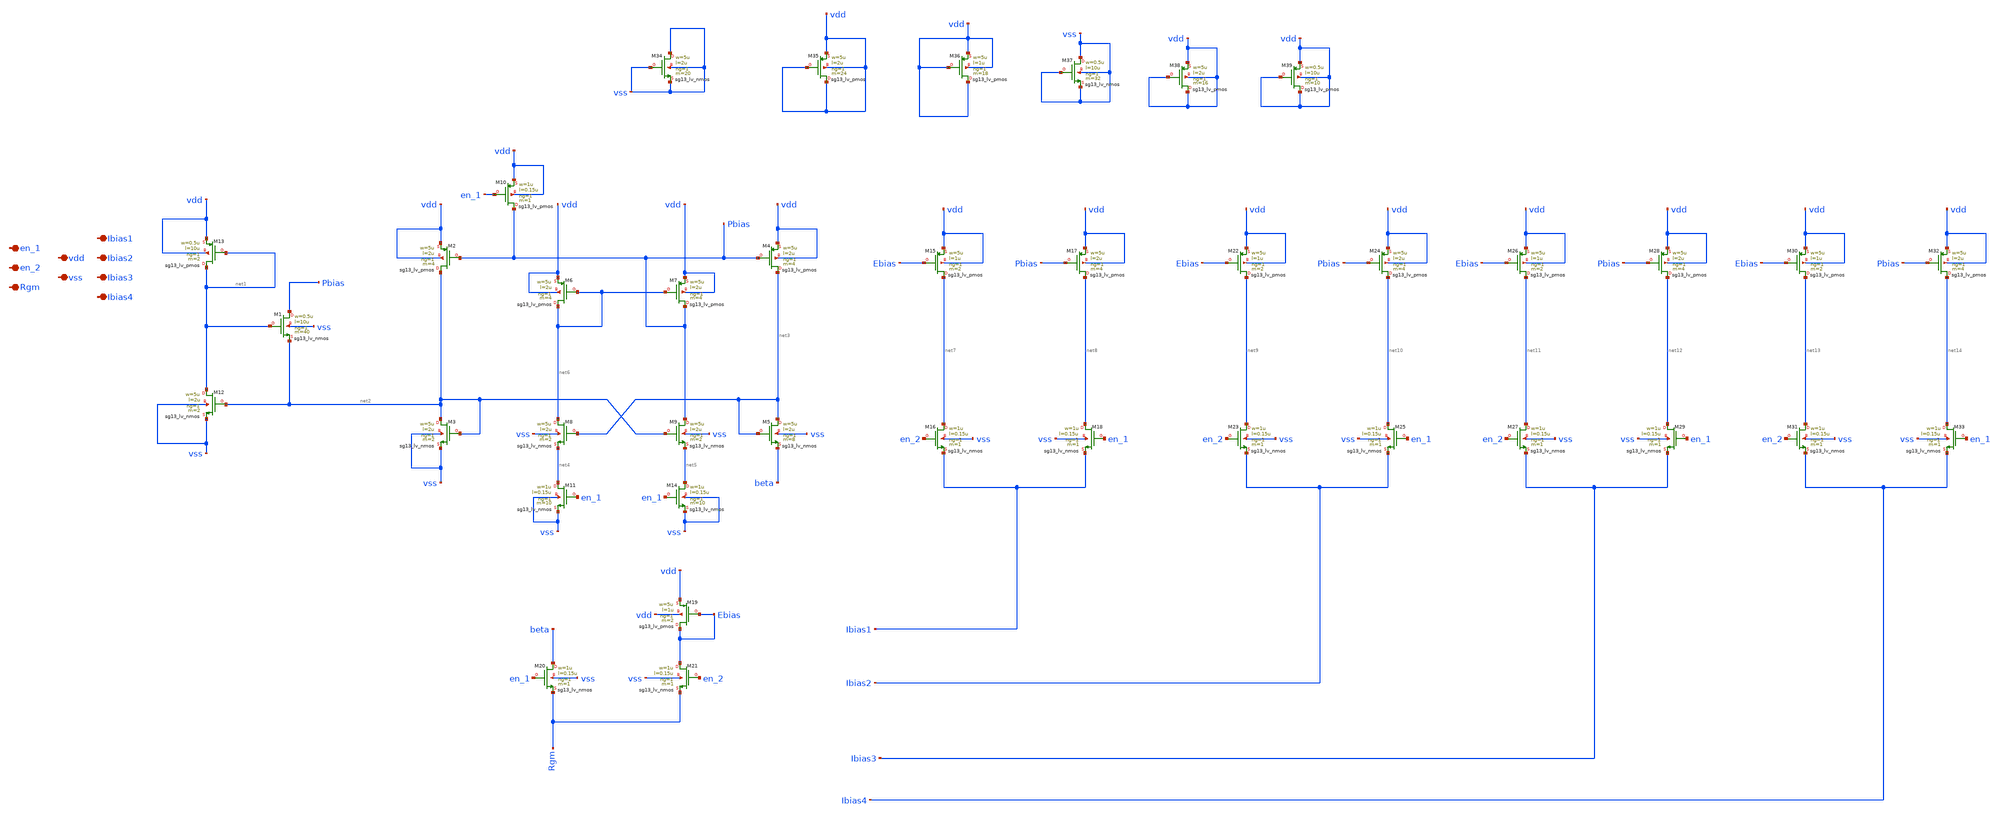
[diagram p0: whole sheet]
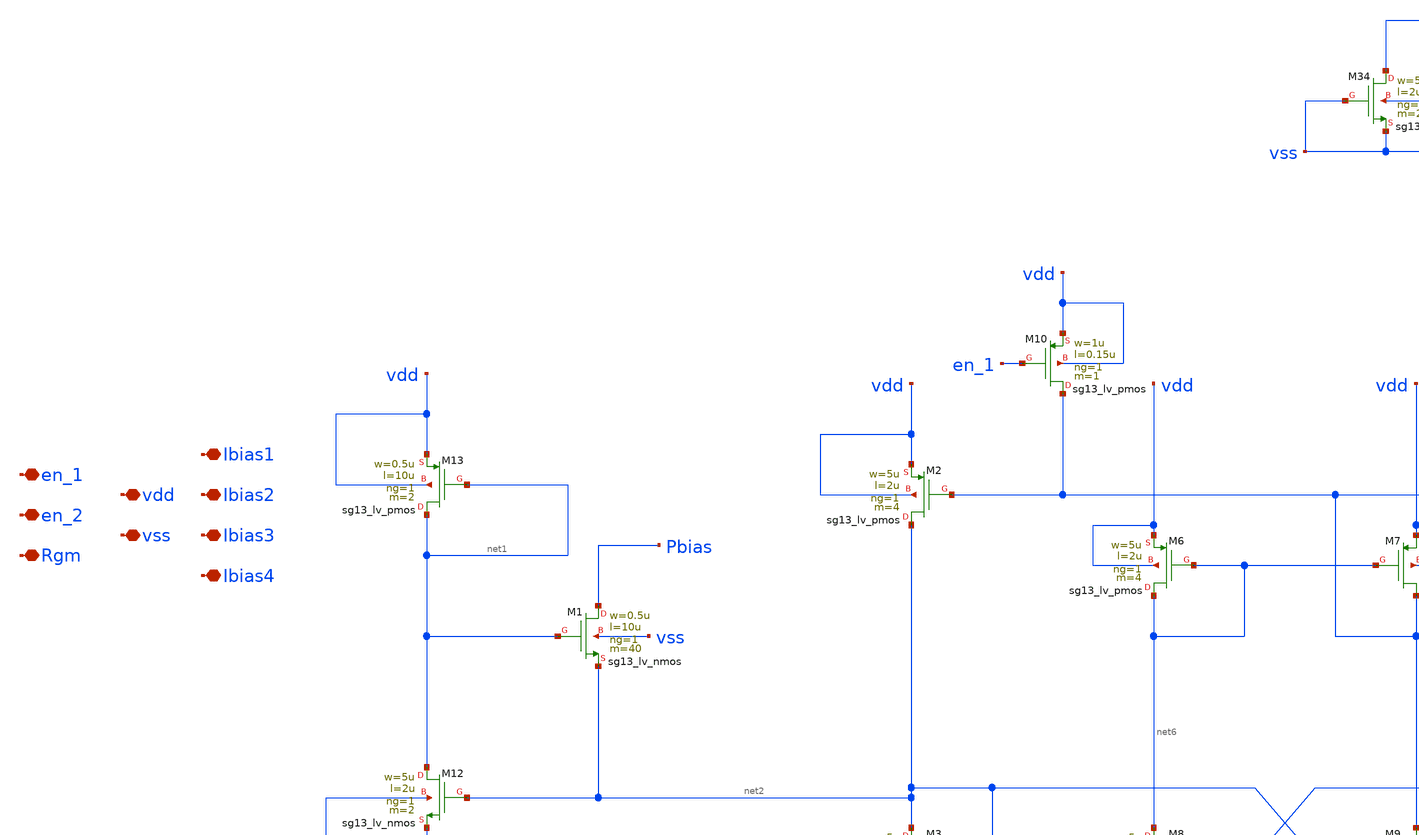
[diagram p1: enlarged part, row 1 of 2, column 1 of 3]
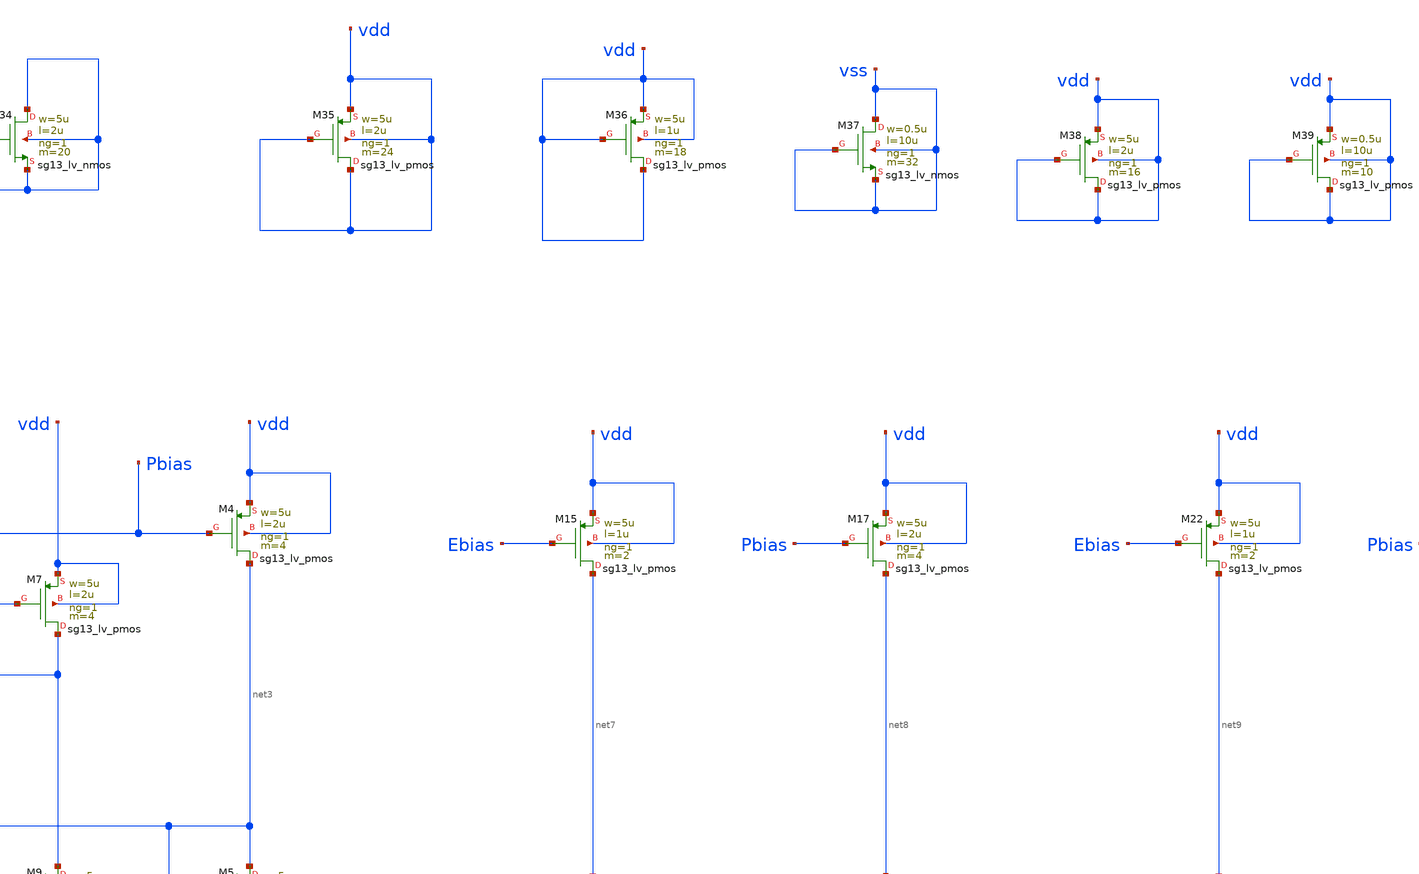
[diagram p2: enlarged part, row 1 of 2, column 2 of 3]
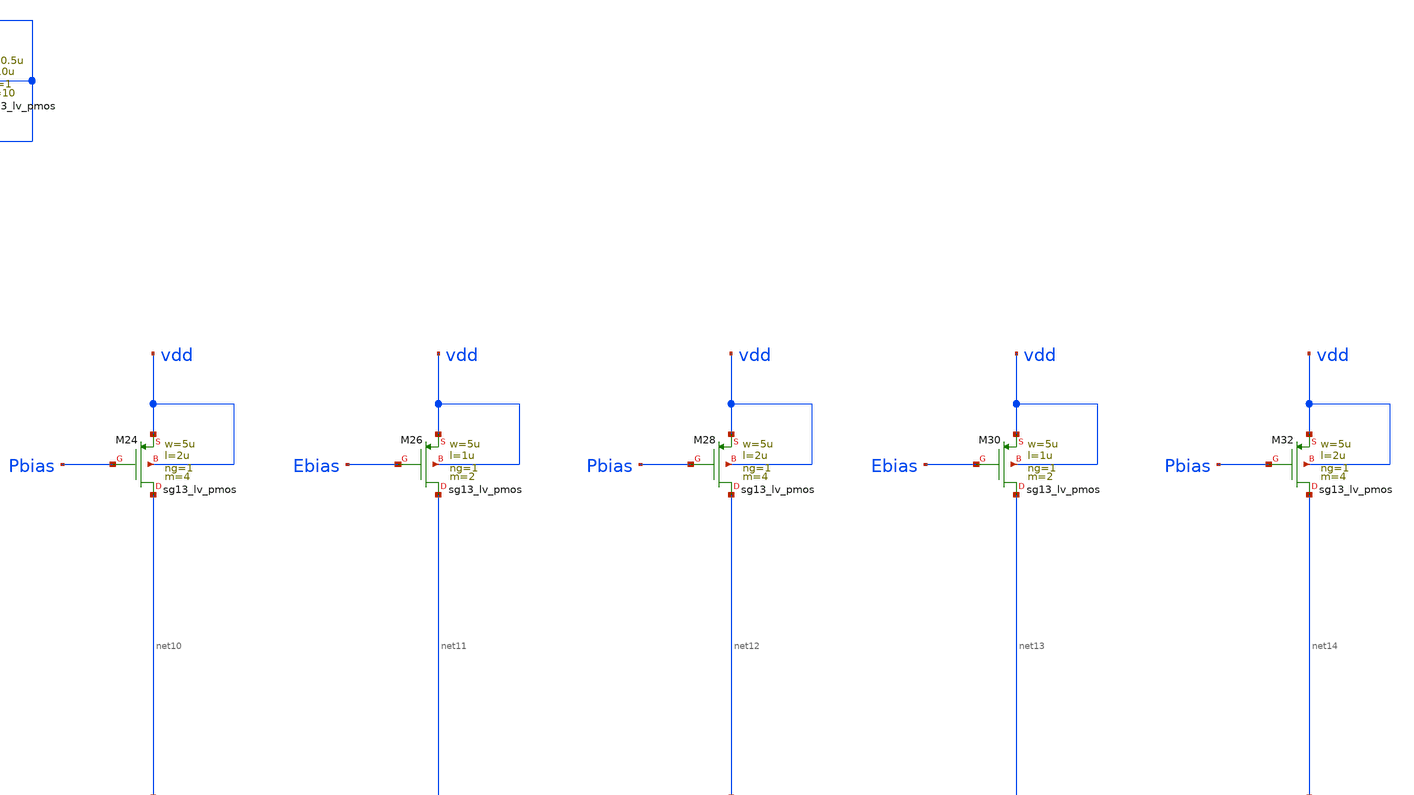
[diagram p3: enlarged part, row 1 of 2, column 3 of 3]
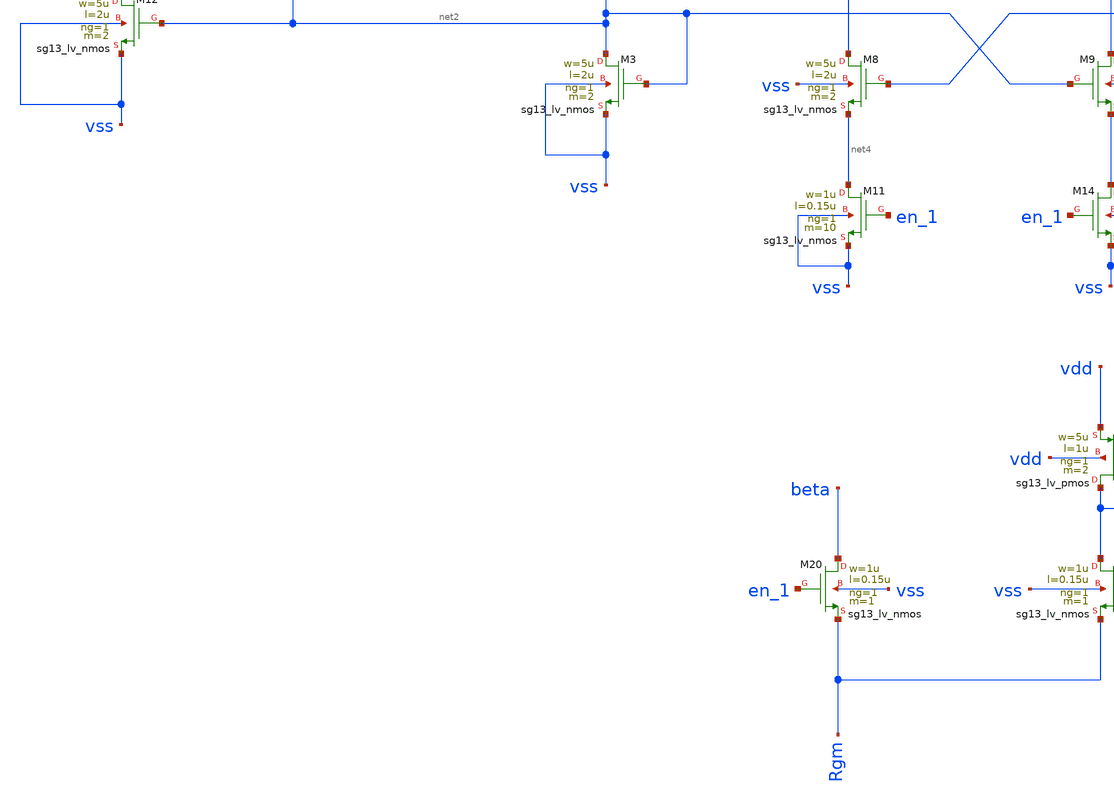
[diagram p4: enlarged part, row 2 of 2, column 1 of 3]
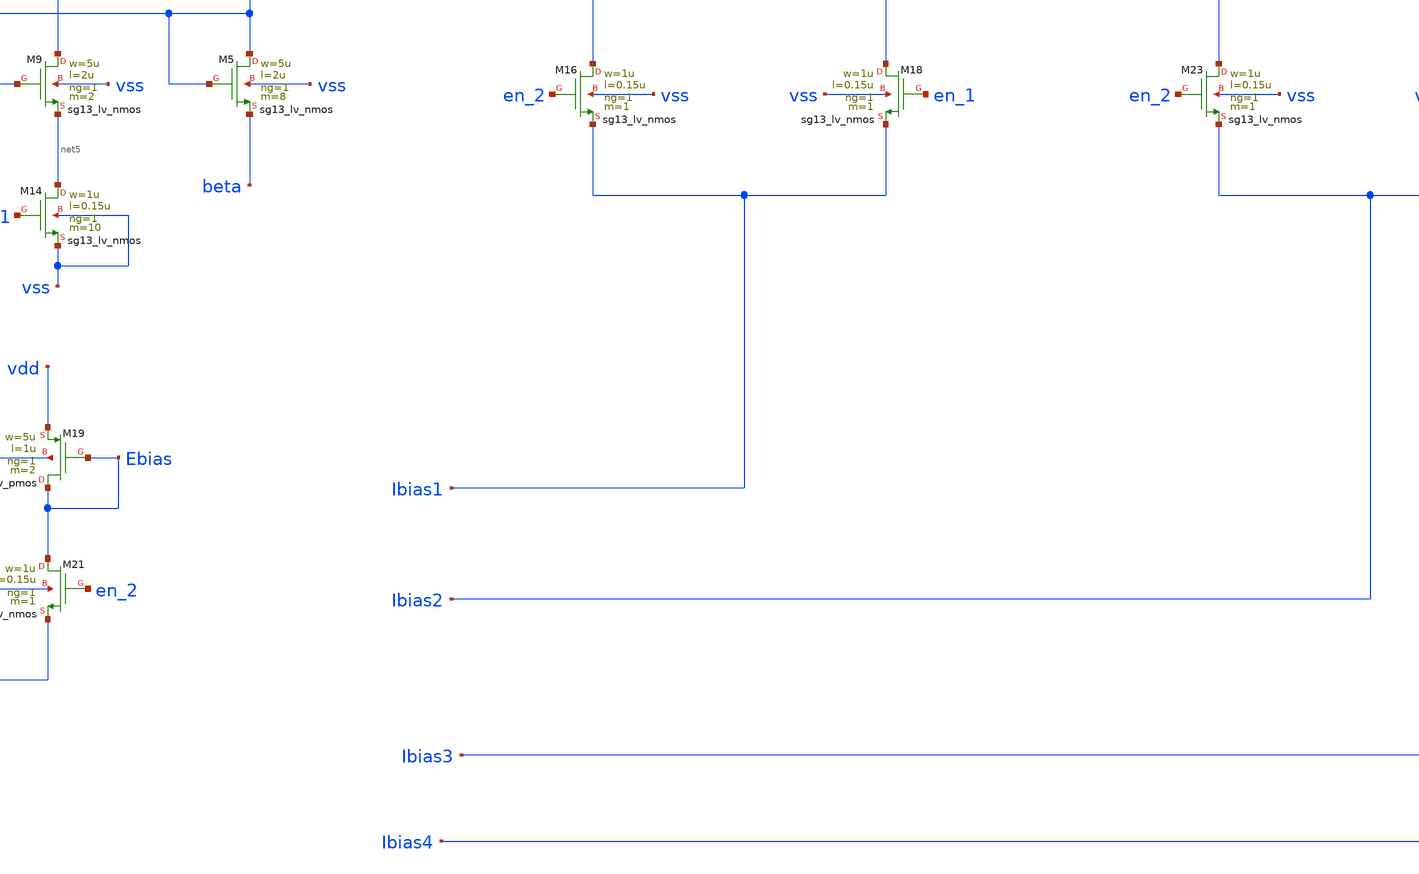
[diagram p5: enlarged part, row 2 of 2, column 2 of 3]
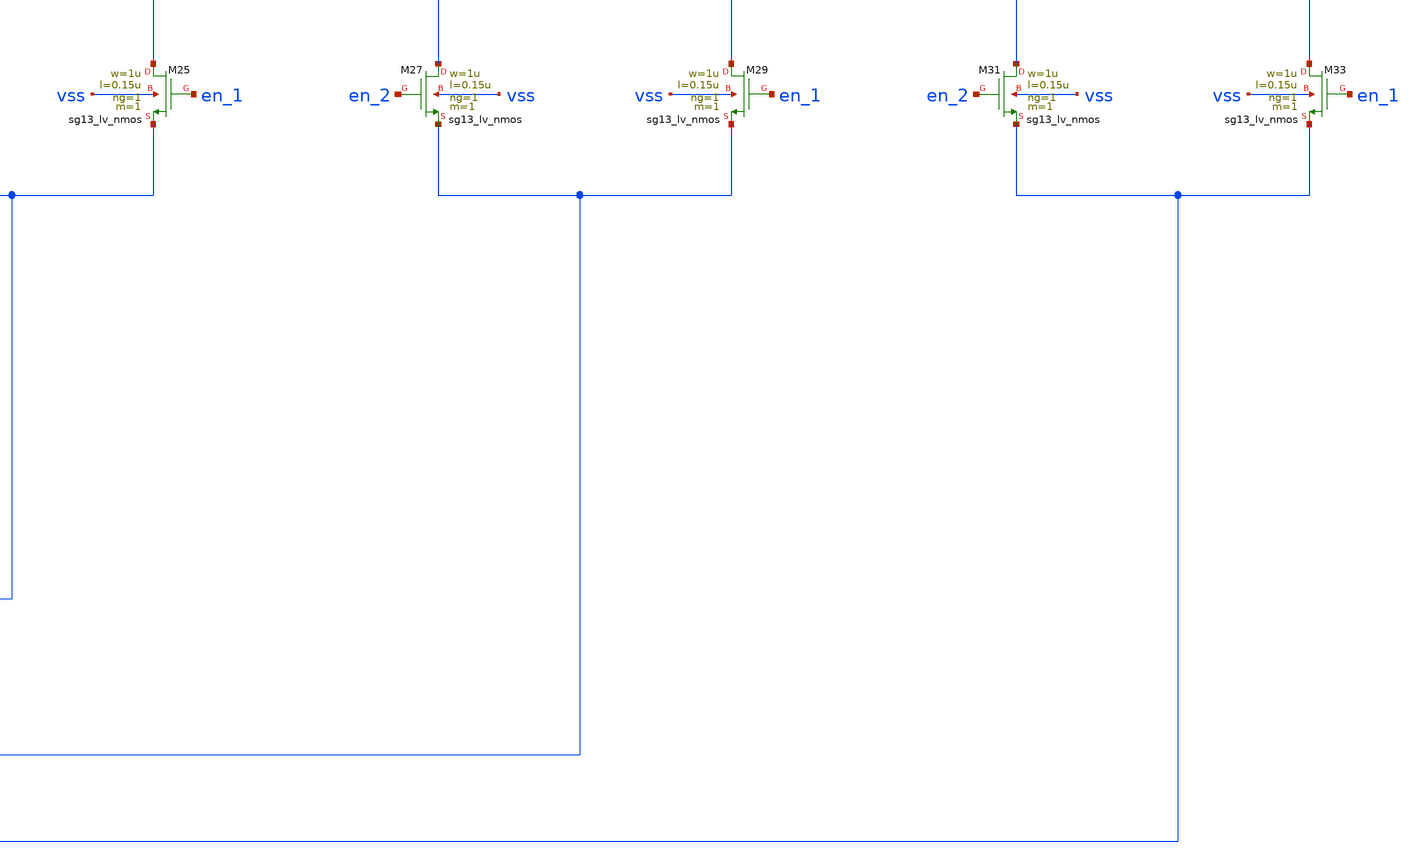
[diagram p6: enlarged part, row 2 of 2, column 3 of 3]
** sch_path: LVS/Unic_cass_final_design_lvs/Simulations/Opamp_design/Src/Bias_circuit.sch
**.subckt Bias_circuit en_1 en_2 Rgm vdd vss Ibias1 Ibias2 Ibias3 Ibias4
*.iopin en_1
*.iopin en_2
*.iopin Rgm
*.iopin vdd
*.iopin vss
*.iopin Ibias1
*.iopin Ibias2
*.iopin Ibias3
*.iopin Ibias4
XM12 net1 net2 vss vss sg13_lv_nmos w=5u l=2u ng=1 m=2 mm_ok=1
XM13 net1 net1 vdd vdd sg13_lv_pmos w=0.5u l=10u ng=1 m=2 mm_ok=1
XM1 Pbias net1 net2 vss sg13_lv_nmos w=0.5u l=10u ng=1 m=40 mm_ok=1
XM2 net2 Pbias vdd vdd sg13_lv_pmos w=5u l=2u ng=1 m=4 mm_ok=1
XM3 net2 net2 vss vss sg13_lv_nmos w=5u l=2u ng=1 m=2 mm_ok=1
XM4 net3 Pbias vdd vdd sg13_lv_pmos w=5u l=2u ng=1 m=4 mm_ok=1
XM5 net3 net3 beta vss sg13_lv_nmos w=5u l=2u ng=1 m=8 mm_ok=1
XM6 net6 net6 vdd vdd sg13_lv_pmos w=5u l=2u ng=1 m=4 mm_ok=1
XM7 Pbias net6 vdd vdd sg13_lv_pmos w=5u l=2u ng=1 m=4 mm_ok=1
XM8 net6 net3 net4 vss sg13_lv_nmos w=5u l=2u ng=1 m=2 mm_ok=1
XM9 Pbias net2 net5 vss sg13_lv_nmos w=5u l=2u ng=1 m=2 mm_ok=1
XM10 Pbias en_1 vdd vdd sg13_lv_pmos w=1u l=0.15u ng=1 m=1 mm_ok=1
XM11 net4 en_1 vss vss sg13_lv_nmos w=1u l=0.15u ng=1 m=10 mm_ok=1
XM14 net5 en_1 vss vss sg13_lv_nmos w=1u l=0.15u ng=1 m=10 mm_ok=1
XM15 net7 Ebias vdd vdd sg13_lv_pmos w=5u l=1u ng=1 m=2 mm_ok=1
XM16 net7 en_2 Ibias1 vss sg13_lv_nmos w=1u l=0.15u ng=1 m=1 mm_ok=1
XM17 net8 Pbias vdd vdd sg13_lv_pmos w=5u l=2u ng=1 m=4 mm_ok=1
XM18 net8 en_1 Ibias1 vss sg13_lv_nmos w=1u l=0.15u ng=1 m=1 mm_ok=1
XM19 Ebias Ebias vdd vdd sg13_lv_pmos w=5u l=1u ng=1 m=2 mm_ok=1
XM20 beta en_1 Rgm vss sg13_lv_nmos w=1u l=0.15u ng=1 m=1 mm_ok=1
XM21 Ebias en_2 Rgm vss sg13_lv_nmos w=1u l=0.15u ng=1 m=1 mm_ok=1
XM22 net9 Ebias vdd vdd sg13_lv_pmos w=5u l=1u ng=1 m=2 mm_ok=1
XM23 net9 en_2 Ibias2 vss sg13_lv_nmos w=1u l=0.15u ng=1 m=1 mm_ok=1
XM24 net10 Pbias vdd vdd sg13_lv_pmos w=5u l=2u ng=1 m=4 mm_ok=1
XM25 net10 en_1 Ibias2 vss sg13_lv_nmos w=1u l=0.15u ng=1 m=1 mm_ok=1
XM26 net11 Ebias vdd vdd sg13_lv_pmos w=5u l=1u ng=1 m=2 mm_ok=1
XM27 net11 en_2 Ibias3 vss sg13_lv_nmos w=1u l=0.15u ng=1 m=1 mm_ok=1
XM28 net12 Pbias vdd vdd sg13_lv_pmos w=5u l=2u ng=1 m=4 mm_ok=1
XM29 net12 en_1 Ibias3 vss sg13_lv_nmos w=1u l=0.15u ng=1 m=1 mm_ok=1
XM30 net13 Ebias vdd vdd sg13_lv_pmos w=5u l=1u ng=1 m=2 mm_ok=1
XM31 net13 en_2 Ibias4 vss sg13_lv_nmos w=1u l=0.15u ng=1 m=1 mm_ok=1
XM32 net14 Pbias vdd vdd sg13_lv_pmos w=5u l=2u ng=1 m=4 mm_ok=1
XM33 net14 en_1 Ibias4 vss sg13_lv_nmos w=1u l=0.15u ng=1 m=1 mm_ok=1
XM34 vss vss vss vss sg13_lv_nmos w=5u l=2u ng=1 m=20 mm_ok=1
XM35 vdd vdd vdd vdd sg13_lv_pmos w=5u l=2u ng=1 m=24 mm_ok=1
XM36 vdd vdd vdd vdd sg13_lv_pmos w=5u l=1u ng=1 m=18 mm_ok=1
XM37 vss vss vss vss sg13_lv_nmos w=0.5u l=10u ng=1 m=32 mm_ok=1
XM38 vdd vdd vdd vdd sg13_lv_pmos w=5u l=2u ng=1 m=16 mm_ok=1
XM39 vdd vdd vdd vdd sg13_lv_pmos w=0.5u l=10u ng=1 m=10 mm_ok=1
**.ends
.end
